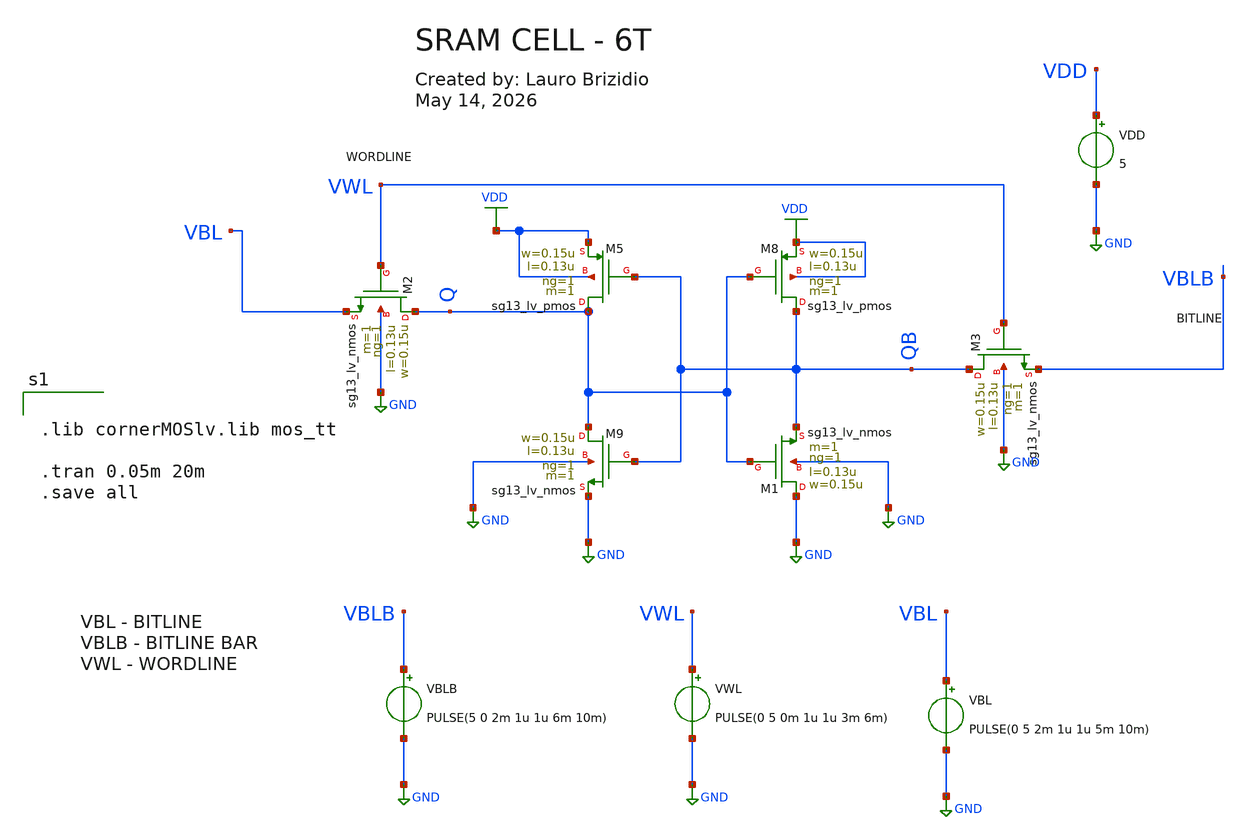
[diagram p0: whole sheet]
** sch_path: projetofinal/shared/schematic_sram/SRAM.sch
**.subckt SRAM
VBL VBL GND PULSE(0 5 2m 1u 1u 5m 10m)
VWL VWL GND PULSE(0 5 0m 1u 1u 3m 6m)
VDD VDD GND 5
VBLB VBLB GND PULSE(5 0 2m 1u 1u 6m 10m)
XM5 Q QB VDD VDD sg13_lv_pmos w=0.15u l=0.13u ng=1 m=1 mm_ok=1
XM9 Q QB GND GND sg13_lv_nmos w=0.15u l=0.13u ng=1 m=1 mm_ok=1
XM8 QB Q VDD VDD sg13_lv_pmos w=0.15u l=0.13u ng=1 m=1 mm_ok=1
XM1 GND Q QB GND sg13_lv_nmos w=0.15u l=0.13u ng=1 m=1 mm_ok=1
XM2 Q VWL VBL GND sg13_lv_nmos w=0.15u l=0.13u ng=1 m=1 mm_ok=1
XM3 QB VWL VBLB GND sg13_lv_nmos w=0.15u l=0.13u ng=1 m=1 mm_ok=1
**** begin user architecture code


.lib cornerMOSlv.lib mos_tt

.tran 0.05m 20m
.save all


**** end user architecture code
**.ends
.GLOBAL VDD
.GLOBAL GND
.end
